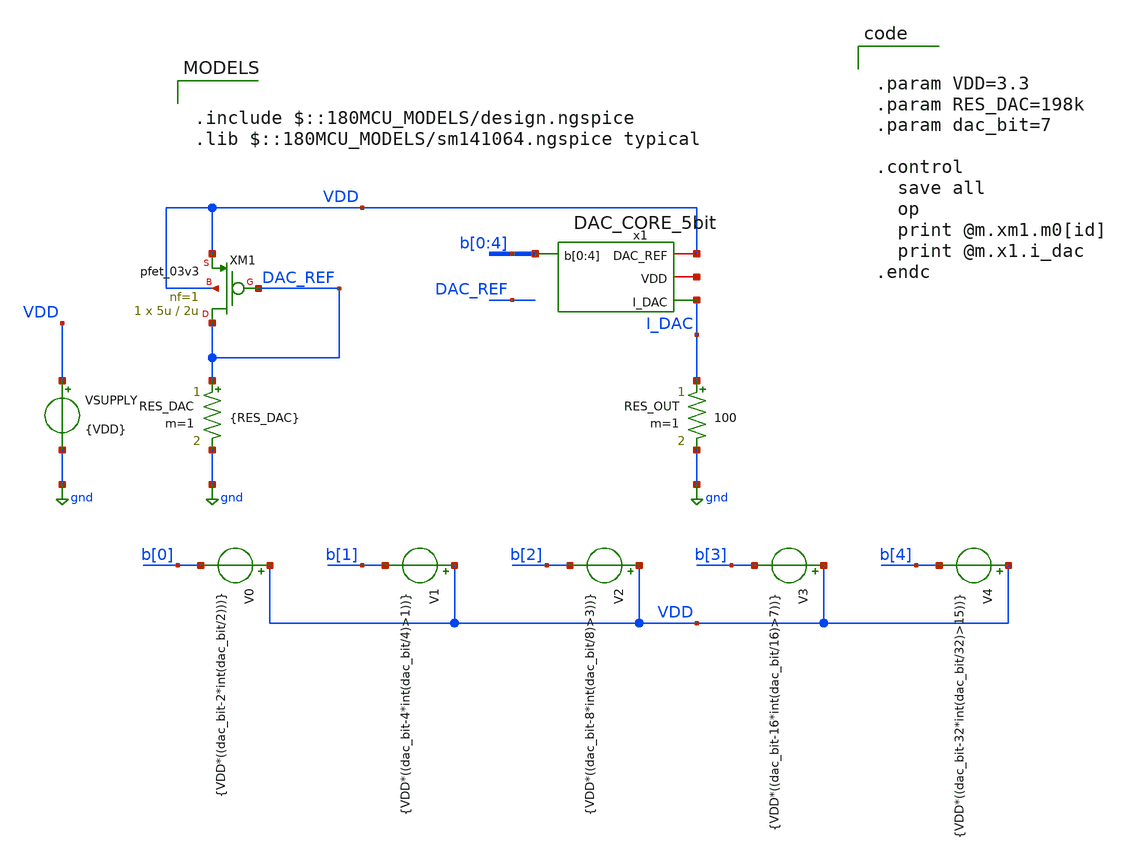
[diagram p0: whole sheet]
** sch_path: DAC_CORE_5bit/DAC_CORE_5bit_test.sch
**.subckt DAC_CORE_5bit_test
x1 VDD net1 b[0] b[1] b[2] b[3] b[4] I_DAC DAC_CORE_5bit
XM1 DAC_REF DAC_REF VDD VDD pfet_03v3 L=2u W=5u nf=1 ad='int((nf+1)/2) * W/nf * 0.18u' as='int((nf+2)/2) * W/nf * 0.18u'
+ pd='2*int((nf+1)/2) * (W/nf + 0.18u)' ps='2*int((nf+2)/2) * (W/nf + 0.18u)' nrd='0.18u / W' nrs='0.18u / W'
+ sa=0 sb=0 sd=0 m=1
RES_DAC DAC_REF gnd {RES_DAC} m=1
RES_OUT I_DAC gnd 100 m=1
V0 VDD b[0] {VDD*((dac_bit-2*int(dac_bit/2)))}
VSUPPLY VDD gnd {VDD}
V1 VDD b[1] {VDD*((dac_bit-4*int(dac_bit/4)>1))}
V2 VDD b[2] {VDD*((dac_bit-8*int(dac_bit/8)>3))}
V3 VDD b[3] {VDD*((dac_bit-16*int(dac_bit/16)>7))}
V4 VDD b[4] {VDD*((dac_bit-32*int(dac_bit/32)>15))}
**** begin user architecture code


.param VDD=3.3
.param RES_DAC=198k
.param dac_bit=7

.control
  save all
  op
  print @m.xm1.m0[id]
  print @m.x1.i_dac
.endc



.include $::180MCU_MODELS/design.ngspice
.lib $::180MCU_MODELS/sm141064.ngspice typical

**** end user architecture code
**.ends

* expanding   symbol:  DAC_CORE_5bit.sym # of pins=4
** sym_path: DAC_CORE_5bit/DAC_CORE_5bit.sym
** sch_path: DAC_CORE_5bit/DAC_CORE_5bit.sch
.subckt DAC_CORE_5bit DAC_REF VDD b[0] b[1] b[2] b[3] b[4] I_DAC
*.opin I_DAC
*.iopin VDD
*.iopin DAC_REF
*.ipin b[0],b[1],b[2],b[3],b[4]
XMK1 I_DAC b[0] net5 VDD pfet_03v3 L=0.28u W=0.78u nf=1 ad='int((nf+1)/2) * W/nf * 0.18u' as='int((nf+2)/2) * W/nf * 0.18u'
+ pd='2*int((nf+1)/2) * (W/nf + 0.18u)' ps='2*int((nf+2)/2) * (W/nf + 0.18u)' nrd='0.18u / W' nrs='0.18u / W'
+ sa=0 sb=0 sd=0 m=1
XMK2 I_DAC b[1] net1 VDD pfet_03v3 L=0.28u W=0.78u nf=1 ad='int((nf+1)/2) * W/nf * 0.18u' as='int((nf+2)/2) * W/nf * 0.18u'
+ pd='2*int((nf+1)/2) * (W/nf + 0.18u)' ps='2*int((nf+2)/2) * (W/nf + 0.18u)' nrd='0.18u / W' nrs='0.18u / W'
+ sa=0 sb=0 sd=0 m=2
XMK3 I_DAC b[2] net2 VDD pfet_03v3 L=0.28u W=0.78u nf=1 ad='int((nf+1)/2) * W/nf * 0.18u' as='int((nf+2)/2) * W/nf * 0.18u'
+ pd='2*int((nf+1)/2) * (W/nf + 0.18u)' ps='2*int((nf+2)/2) * (W/nf + 0.18u)' nrd='0.18u / W' nrs='0.18u / W'
+ sa=0 sb=0 sd=0 m=4
XMK4 I_DAC b[3] net3 VDD pfet_03v3 L=0.28u W=0.78u nf=1 ad='int((nf+1)/2) * W/nf * 0.18u' as='int((nf+2)/2) * W/nf * 0.18u'
+ pd='2*int((nf+1)/2) * (W/nf + 0.18u)' ps='2*int((nf+2)/2) * (W/nf + 0.18u)' nrd='0.18u / W' nrs='0.18u / W'
+ sa=0 sb=0 sd=0 m=8
XMK5 I_DAC b[4] net4 VDD pfet_03v3 L=0.28u W=0.78u nf=1 ad='int((nf+1)/2) * W/nf * 0.18u' as='int((nf+2)/2) * W/nf * 0.18u'
+ pd='2*int((nf+1)/2) * (W/nf + 0.18u)' ps='2*int((nf+2)/2) * (W/nf + 0.18u)' nrd='0.18u / W' nrs='0.18u / W'
+ sa=0 sb=0 sd=0 m=16
XM1 net5 DAC_REF VDD VDD pfet_03v3 L=2u W=5u nf=1 ad='int((nf+1)/2) * W/nf * 0.18u' as='int((nf+2)/2) * W/nf * 0.18u'
+ pd='2*int((nf+1)/2) * (W/nf + 0.18u)' ps='2*int((nf+2)/2) * (W/nf + 0.18u)' nrd='0.18u / W' nrs='0.18u / W'
+ sa=0 sb=0 sd=0 m=1
XM2 net1 DAC_REF VDD VDD pfet_03v3 L=2u W=5u nf=1 ad='int((nf+1)/2) * W/nf * 0.18u' as='int((nf+2)/2) * W/nf * 0.18u'
+ pd='2*int((nf+1)/2) * (W/nf + 0.18u)' ps='2*int((nf+2)/2) * (W/nf + 0.18u)' nrd='0.18u / W' nrs='0.18u / W'
+ sa=0 sb=0 sd=0 m=2
XM3 net2 DAC_REF VDD VDD pfet_03v3 L=2u W=5u nf=1 ad='int((nf+1)/2) * W/nf * 0.18u' as='int((nf+2)/2) * W/nf * 0.18u'
+ pd='2*int((nf+1)/2) * (W/nf + 0.18u)' ps='2*int((nf+2)/2) * (W/nf + 0.18u)' nrd='0.18u / W' nrs='0.18u / W'
+ sa=0 sb=0 sd=0 m=4
XM4 net3 DAC_REF VDD VDD pfet_03v3 L=2u W=5u nf=1 ad='int((nf+1)/2) * W/nf * 0.18u' as='int((nf+2)/2) * W/nf * 0.18u'
+ pd='2*int((nf+1)/2) * (W/nf + 0.18u)' ps='2*int((nf+2)/2) * (W/nf + 0.18u)' nrd='0.18u / W' nrs='0.18u / W'
+ sa=0 sb=0 sd=0 m=8
XM5 net4 DAC_REF VDD VDD pfet_03v3 L=2u W=5u nf=1 ad='int((nf+1)/2) * W/nf * 0.18u' as='int((nf+2)/2) * W/nf * 0.18u'
+ pd='2*int((nf+1)/2) * (W/nf + 0.18u)' ps='2*int((nf+2)/2) * (W/nf + 0.18u)' nrd='0.18u / W' nrs='0.18u / W'
+ sa=0 sb=0 sd=0 m=16
.ends

.GLOBAL gnd
.end
